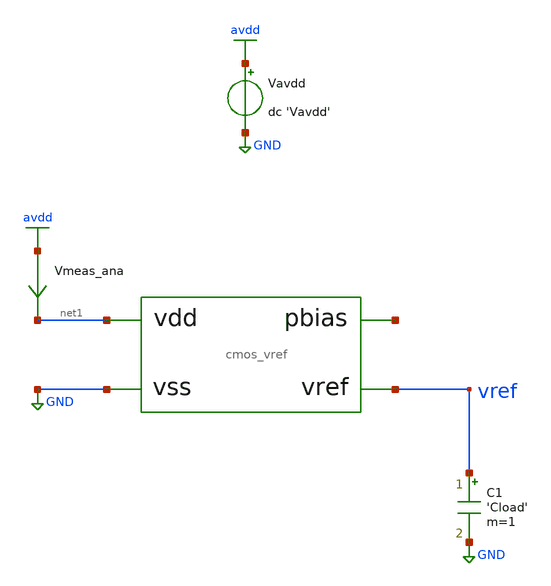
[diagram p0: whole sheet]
** sch_path: tb/cmos_vref/tb_vref_power.sch
**.subckt tb_vref_power
Vavdd avdd GND dc 'Vavdd'
C1 vref GND 'Cload' m=1
Vmeas_ana avdd net1 0
.save i(vmeas_ana)
X1 vref net1 GND net2 cmos_vref
**** begin user architecture code


.lib 'models_dir'/cornerMOShv.lib 'mos_corner'
.lib 'models_dir'/cornerMOSlv.lib 'mos_corner'
.lib 'models_dir'/cornerCAP.lib cap_typ
.option TEMP='temperature'
.option warn=1
.option savecurrents
.control
save all
op
print I(Vmeas_ana), I(Vavdd)
set wr_singlescale
wrdata 'simpath'/'filename'_'N'.data -I(Vavdd)
quit
.endc


**** end user architecture code
**.ends
.GLOBAL avdd
.GLOBAL GND
.end
